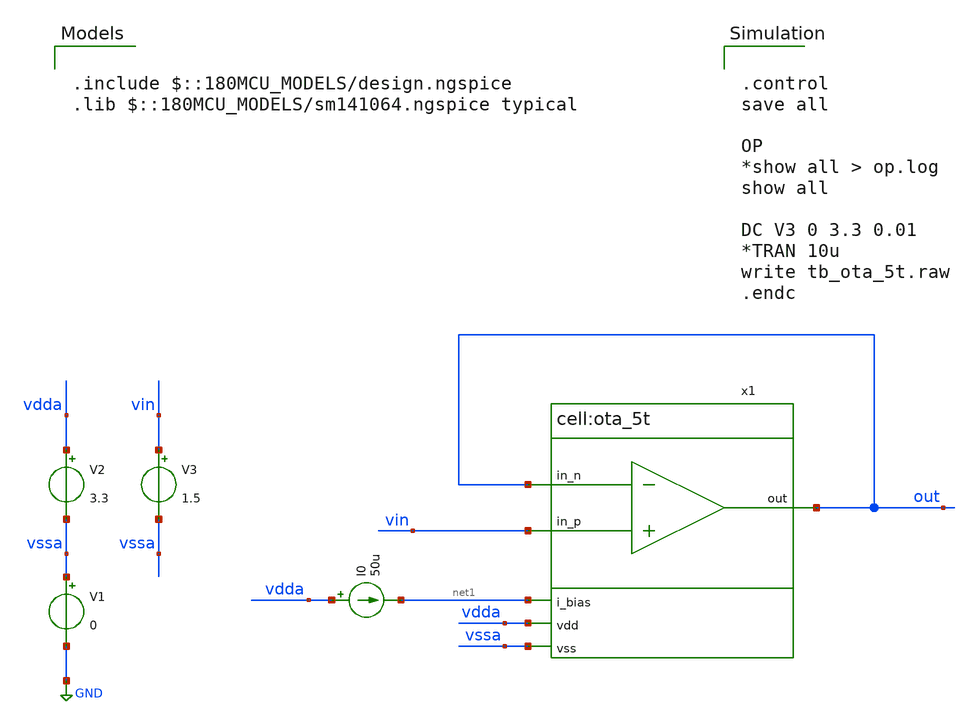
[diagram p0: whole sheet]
** sch_path: designs/libs/xp_tb_analog/tb_ota_5t_dc/tb_ota_5t_dc.sch
**.subckt tb_ota_5t_dc
V1 vssa GND 0
V2 vdda vssa 3.3
I0 vdda net1 50u
V3 vin vssa 1.5
x1 vdda out vin out net1 vssa ota_5t
**** begin user architecture code


.control
save all

OP
*show all > op.log
show all

DC V3 0 3.3 0.01
*TRAN 10u
write tb_ota_5t.raw
.endc



.include $::180MCU_MODELS/design.ngspice
.lib $::180MCU_MODELS/sm141064.ngspice typical

**** end user architecture code
**.ends
.GLOBAL GND
.end
